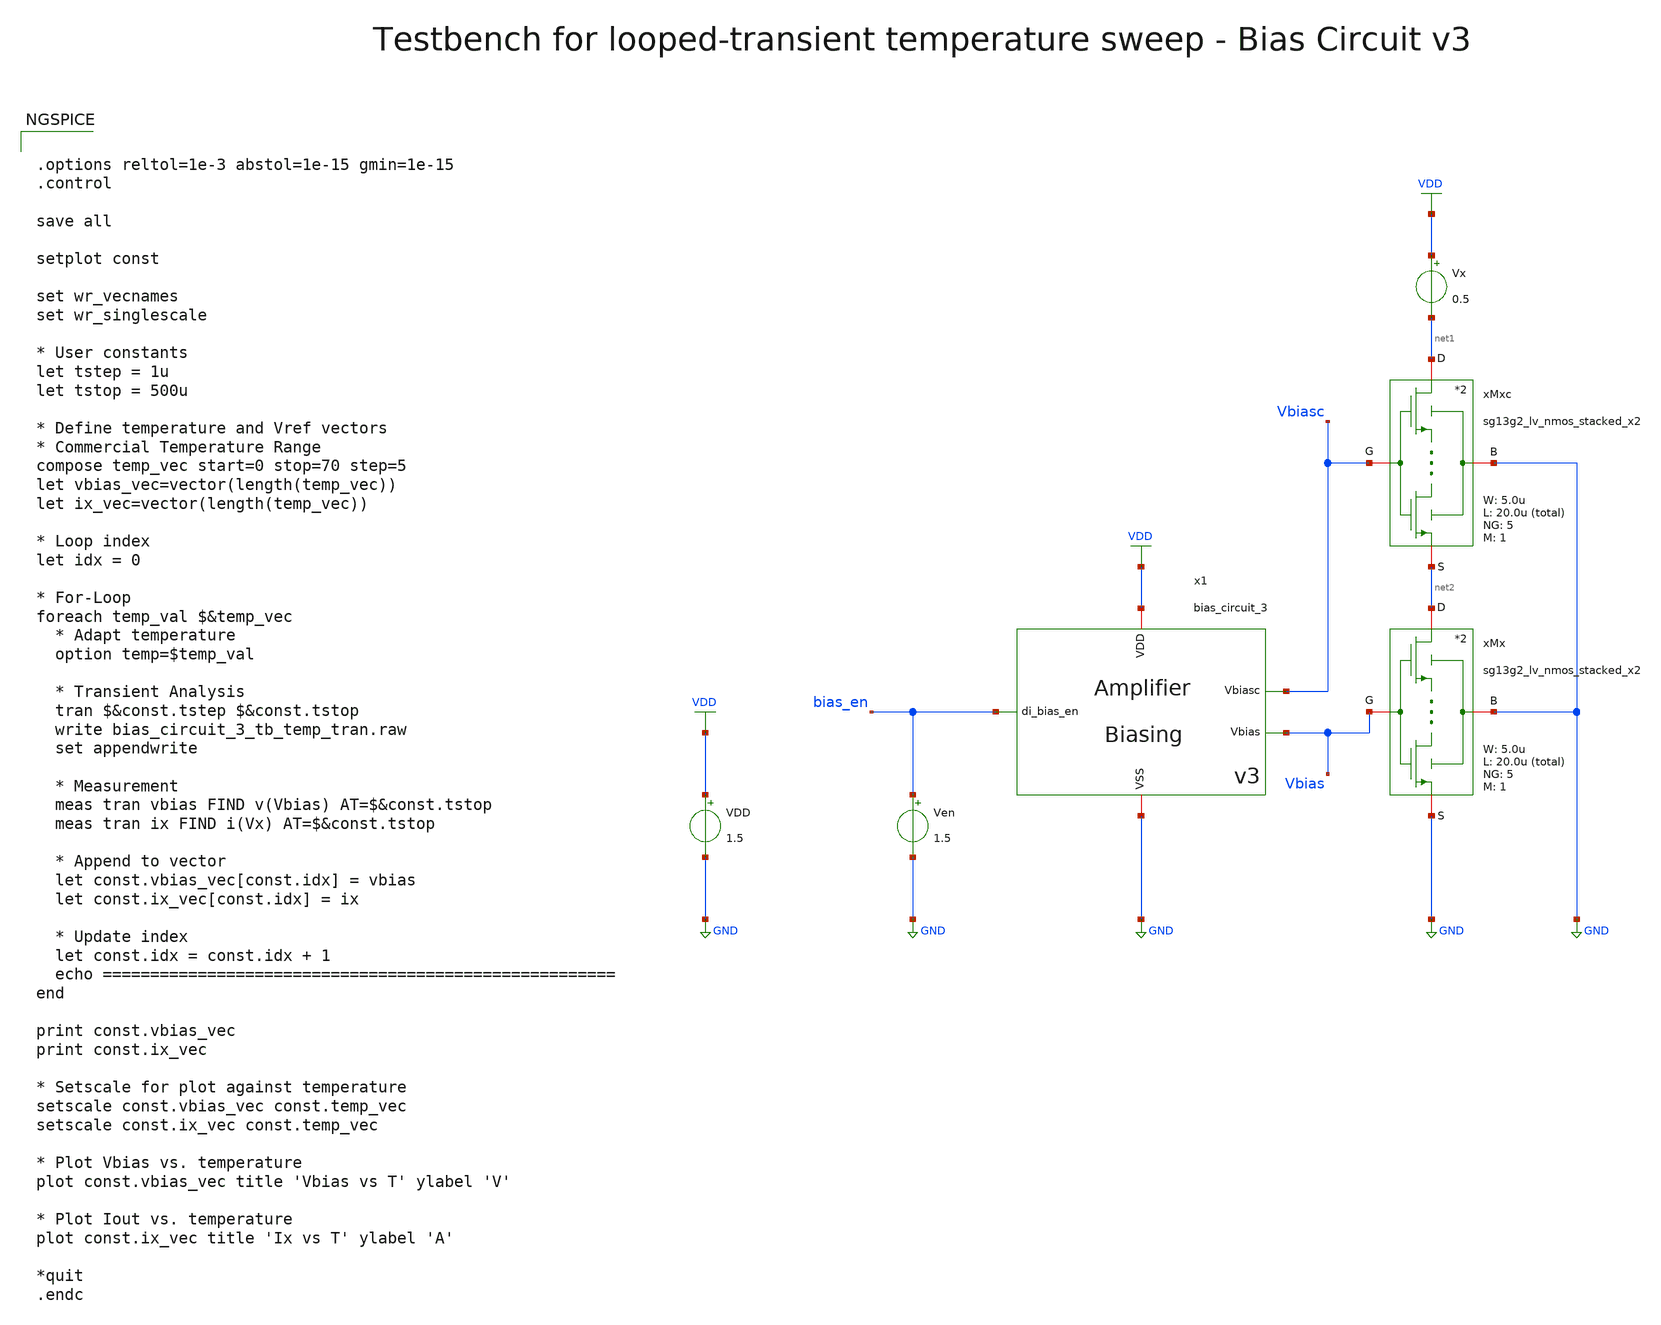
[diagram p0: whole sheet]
** sch_path: SG13G2_ATBS-ADC-main/xschem/bio_amplifier/amplifier_core/bias_circuit/bias_circuit_3/testbenches/bias_circuit_3_tb_temp_tran.sch
**.subckt bias_circuit_3_tb_temp_tran
Ven bias_en GND 1.5
VDD VDD GND 1.5
x1 bias_en VDD GND Vbias Vbiasc bias_circuit_3
Vx VDD net1 0.5
xMx net2 Vbias GND GND sg13g2_lv_nmos_stacked_x2 W_N=5.0u L_N=20.0u NG_N=5 M_N=1
xMxc net1 Vbiasc GND net2 sg13g2_lv_nmos_stacked_x2 W_N=5.0u L_N=20.0u NG_N=5 M_N=1
**** begin user architecture code

.lib cornerMOSlv.lib mos_tt
.lib cornerRES.lib res_typ



.options reltol=1e-3 abstol=1e-15 gmin=1e-15
.control

save all

setplot const

set wr_vecnames
set wr_singlescale

* User constants
let tstep = 1u
let tstop = 500u

* Define temperature and Vref vectors
* Commercial Temperature Range
compose temp_vec start=0 stop=70 step=5
let vbias_vec=vector(length(temp_vec))
let ix_vec=vector(length(temp_vec))

* Loop index
let idx = 0

* For-Loop
foreach temp_val $&temp_vec
  * Adapt temperature
  option temp=$temp_val

  * Transient Analysis
  tran $&const.tstep $&const.tstop
  write bias_circuit_3_tb_temp_tran.raw
  set appendwrite

  * Measurement
  meas tran vbias FIND v(Vbias) AT=$&const.tstop
  meas tran ix FIND i(Vx) AT=$&const.tstop

  * Append to vector
  let const.vbias_vec[const.idx] = vbias
  let const.ix_vec[const.idx] = ix

  * Update index
  let const.idx = const.idx + 1
  echo ======================================================
end

print const.vbias_vec
print const.ix_vec

* Setscale for plot against temperature
setscale const.vbias_vec const.temp_vec
setscale const.ix_vec const.temp_vec

* Plot Vbias vs. temperature
plot const.vbias_vec title 'Vbias vs T' ylabel 'V'

* Plot Iout vs. temperature
plot const.ix_vec title 'Ix vs T' ylabel 'A'

*quit
.endc

**** end user architecture code
**.ends

* expanding   symbol:  bio_amplifier/amplifier_core/bias_circuit/bias_circuit_3/bias_circuit_3.sym #
*+ of pins=5
** sym_path: SG13G2_ATBS-ADC-main/xschem/bio_amplifier/amplifier_core/bias_circuit/bias_circuit_3/bias_circuit_3.sym
** sch_path: SG13G2_ATBS-ADC-main/xschem/bio_amplifier/amplifier_core/bias_circuit/bias_circuit_3/bias_circuit_3.sch
.subckt bias_circuit_3 di_bias_en VDD VSS Vbias Vbiasc
*.iopin VDD
*.iopin VSS
*.opin Vbias
*.ipin di_bias_en
*.opin Vbiasc
XMDEC1 net1 Vbias net1 net1 sg13_lv_nmos w=100.0u l=40.0u ng=100 m=1 mm_ok=1
VIref net4 net7 0
.save i(viref)
VIout net6 Vbiasc 0
.save i(viout)
x1 VDD di_bias_en bias_en_n VSS inverter_lv W_P=1.0u L_P=0.13u W_N=1.0u L_N=0.13u
XMPD1 Vgs_m34 di_bias_en net2 net2 sg13_lv_pmos w=1.0u l=0.13u ng=1 m=1 mm_ok=1
XMPD2 net4 bias_en_n Vgs_m34 net2 sg13_lv_pmos w=1.0u l=0.13u ng=1 m=1 mm_ok=1
VIref5 net1 VSS 0
.save i(viref5)
VIdd VDD net2 0
.save i(vidd)
xM1 net5 net5 VSS net3 sg13g2_lv_nmos_stacked_x2 W_N=20.0u L_N=20.0u NG_N=20 M_N=1
xM1c net7 Vbiasc VSS net5 sg13g2_lv_nmos_stacked_x2 W_N=5.0u L_N=20.0u NG_N=5 M_N=1
xM2 Vbias Vbias VSS VSS sg13g2_lv_nmos_stacked_x2 W_N=5.0u L_N=20.0u NG_N=5 M_N=1
xM2c Vbiasc Vbiasc VSS Vbias sg13g2_lv_nmos_stacked_x2 W_N=5.0u L_N=20.0u NG_N=5 M_N=1
XMDEC2 net2 Vgs_m34 net2 net2 sg13_lv_pmos w=25.0u l=40.0u ng=25 m=1 mm_ok=1
xM3 net4 Vgs_m34 net2 net2 sg13g2_lv_pmos_stacked_x4 W_P=20.0u L_P=40.0u NG_P=20 M_P=1
xM4 net6 Vgs_m34 net2 net2 sg13g2_lv_pmos_stacked_x4 W_P=20.0u L_P=40.0u NG_P=20 M_P=1
x4 di_bias_en Vgs_m34 Vbias net5 VDD VSS aux_ota
R1 net3 VSS 3.521Meg m=1
XMPD3 net5 bias_en_n VSS VSS sg13_lv_nmos w=1.0u l=0.13u ng=1 m=1 mm_ok=1
XMPD4 Vbias bias_en_n VSS VSS sg13_lv_nmos w=1.0u l=0.13u ng=1 m=1 mm_ok=1
xMSU2 Vsu net9 VSS VSS sg13g2_lv_nmos_stacked_x4 W_N=1.0u L_N=40.0u NG_N=1 M_N=1
xMSU1 net8 Vsu VSS net9 sg13g2_lv_nmos_stacked_x4 W_N=1.0u L_N=40.0u NG_N=1 M_N=1
Vmeas1 net4 net8 0
.save i(vmeas1)
Vmeas2 Vbias net9 0
.save i(vmeas2)
CSU1 net10 Vsu 30f m=1
XMPD6 Vsu di_bias_en net10 net10 sg13_lv_pmos w=1.0u l=0.13u ng=1 m=1 mm_ok=1
XMPD7 Vsu bias_en_n VSS VSS sg13_lv_nmos w=1.0u l=0.13u ng=1 m=1 mm_ok=1
XMPD5 net10 bias_en_n net2 net2 sg13_lv_pmos w=1.0u l=0.13u ng=1 m=1 mm_ok=1
.ends


* expanding   symbol:  stacked_transistors/sg13g2_lv_nmos_stacked/sg13g2_lv_nmos_stacked_x2.sym # of
*+ pins=4
** sym_path: SG13G2_ATBS-ADC-main/xschem/stacked_transistors/sg13g2_lv_nmos_stacked/sg13g2_lv_nmos_stacked_x2.sym
** sch_path: SG13G2_ATBS-ADC-main/xschem/stacked_transistors/sg13g2_lv_nmos_stacked/sg13g2_lv_nmos_stacked_x2.sch
.subckt sg13g2_lv_nmos_stacked_x2 D G B S  W_N=1.0u L_N=0.45u NG_N=1 M_N=1
*.iopin D
*.iopin S
*.iopin G
*.iopin B
XM1 net1 G S B sg13_lv_nmos w=W_N l=L_N/2 ng=NG_N m=M_N mm_ok=1
XM2 D G net1 B sg13_lv_nmos w=W_N l=L_N/2 ng=NG_N m=M_N mm_ok=1
.ends


* expanding   symbol:  inverter/inverter_lv.sym # of pins=4
** sym_path: SG13G2_ATBS-ADC-main/xschem/inverter/inverter_lv.sym
** sch_path: SG13G2_ATBS-ADC-main/xschem/inverter/inverter_lv.sch
.subckt inverter_lv VDD vin vout VSS  W_P=3.0u L_P=0.13u W_N=1.0u L_N=0.13u
*.ipin vin
*.iopin VDD
*.iopin VSS
*.opin vout
XM1 vout vin VDD VDD sg13_lv_pmos w=W_P l=L_P ng=1 m=1 mm_ok=1
XM2 vout vin VSS VSS sg13_lv_nmos w=W_N l=L_N ng=1 m=1 mm_ok=1
.ends


* expanding   symbol:  stacked_transistors/sg13g2_lv_pmos_stacked/sg13g2_lv_pmos_stacked_x4.sym # of
*+ pins=4
** sym_path: SG13G2_ATBS-ADC-main/xschem/stacked_transistors/sg13g2_lv_pmos_stacked/sg13g2_lv_pmos_stacked_x4.sym
** sch_path: SG13G2_ATBS-ADC-main/xschem/stacked_transistors/sg13g2_lv_pmos_stacked/sg13g2_lv_pmos_stacked_x4.sch
.subckt sg13g2_lv_pmos_stacked_x4 D G B S  W_P=1.0u L_P=0.45u NG_P=1 M_P=1
*.iopin D
*.iopin S
*.iopin G
*.iopin B
XM1 net1 G S B sg13_lv_pmos w=W_P l=L_P/4 ng=NG_P m=M_P mm_ok=1
XM2 net3 G net1 B sg13_lv_pmos w=W_P l=L_P/4 ng=NG_P m=M_P mm_ok=1
XM3 net2 G net3 B sg13_lv_pmos w=W_P l=L_P/4 ng=NG_P m=M_P mm_ok=1
XM4 D G net2 B sg13_lv_pmos w=W_P l=L_P/4 ng=NG_P m=M_P mm_ok=1
.ends


* expanding   symbol:  bio_amplifier/amplifier_core/bias_circuit/aux_ota/aux_ota.sym # of pins=6
** sym_path: SG13G2_ATBS-ADC-main/xschem/bio_amplifier/amplifier_core/bias_circuit/aux_ota/aux_ota.sym
** sch_path: SG13G2_ATBS-ADC-main/xschem/bio_amplifier/amplifier_core/bias_circuit/aux_ota/aux_ota.sch
.subckt aux_ota di_ota_en vout vinn vinp VDD VSS
*.iopin VDD
*.iopin VSS
*.ipin di_ota_en
*.ipin vinp
*.ipin vinn
*.opin vout
xM3 net1 Vgs_ma34 net2 net2 sg13g2_lv_pmos_stacked_x4 W_P=20.0u L_P=40.0u NG_P=20 M_P=1
xM4 vout Vgs_ma34 net2 net2 sg13g2_lv_pmos_stacked_x4 W_P=20.0u L_P=40.0u NG_P=20 M_P=1
xM1 net1 vinp VSS VSS sg13g2_lv_nmos_stacked_x2 W_N=5.0u L_N=40.0u NG_N=5 M_N=1
VIdd VDD net2 0
.save i(vidd)
xM2 vout vinn VSS VSS sg13g2_lv_nmos_stacked_x2 W_N=5.0u L_N=40.0u NG_N=5 M_N=1
XMPD1 Vgs_ma34 di_ota_en net2 net2 sg13_lv_pmos w=1.0u l=0.13u ng=1 m=1 mm_ok=1
XMPD2 net1 ota_en_n Vgs_ma34 net2 sg13_lv_pmos w=1.0u l=0.13u ng=1 m=1 mm_ok=1
x1 VDD di_ota_en ota_en_n VSS inverter_lv W_P=1.0u L_P=0.13u W_N=1.0u L_N=0.13u
.ends


* expanding   symbol:  stacked_transistors/sg13g2_lv_nmos_stacked/sg13g2_lv_nmos_stacked_x4.sym # of
*+ pins=4
** sym_path: SG13G2_ATBS-ADC-main/xschem/stacked_transistors/sg13g2_lv_nmos_stacked/sg13g2_lv_nmos_stacked_x4.sym
** sch_path: SG13G2_ATBS-ADC-main/xschem/stacked_transistors/sg13g2_lv_nmos_stacked/sg13g2_lv_nmos_stacked_x4.sch
.subckt sg13g2_lv_nmos_stacked_x4 D G B S  W_N=1.0u L_N=0.45u NG_N=1 M_N=1
*.iopin D
*.iopin S
*.iopin G
*.iopin B
XM1 net1 G S B sg13_lv_nmos w=W_N l=L_N/4 ng=NG_N m=M_N mm_ok=1
XM2 net3 G net1 B sg13_lv_nmos w=W_N l=L_N/4 ng=NG_N m=M_N mm_ok=1
XM3 net2 G net3 B sg13_lv_nmos w=W_N l=L_N/4 ng=NG_N m=M_N mm_ok=1
XM4 D G net2 B sg13_lv_nmos w=W_N l=L_N/4 ng=NG_N m=M_N mm_ok=1
.ends

.GLOBAL GND
.GLOBAL VDD
.end
